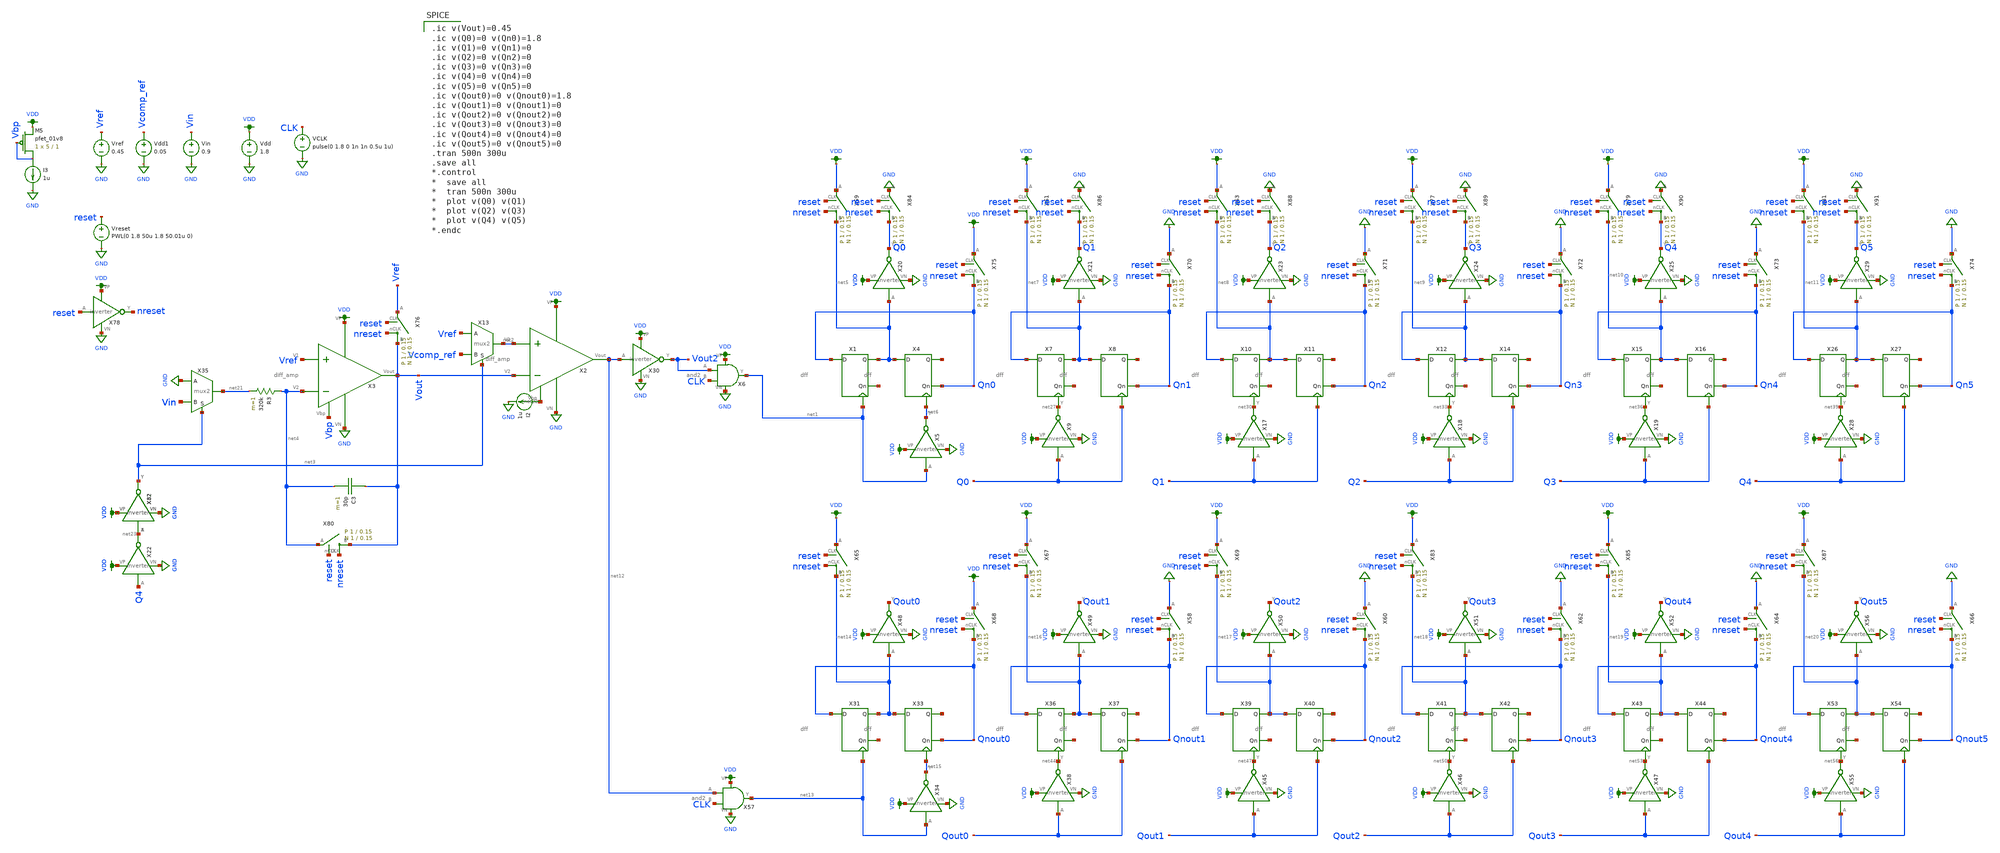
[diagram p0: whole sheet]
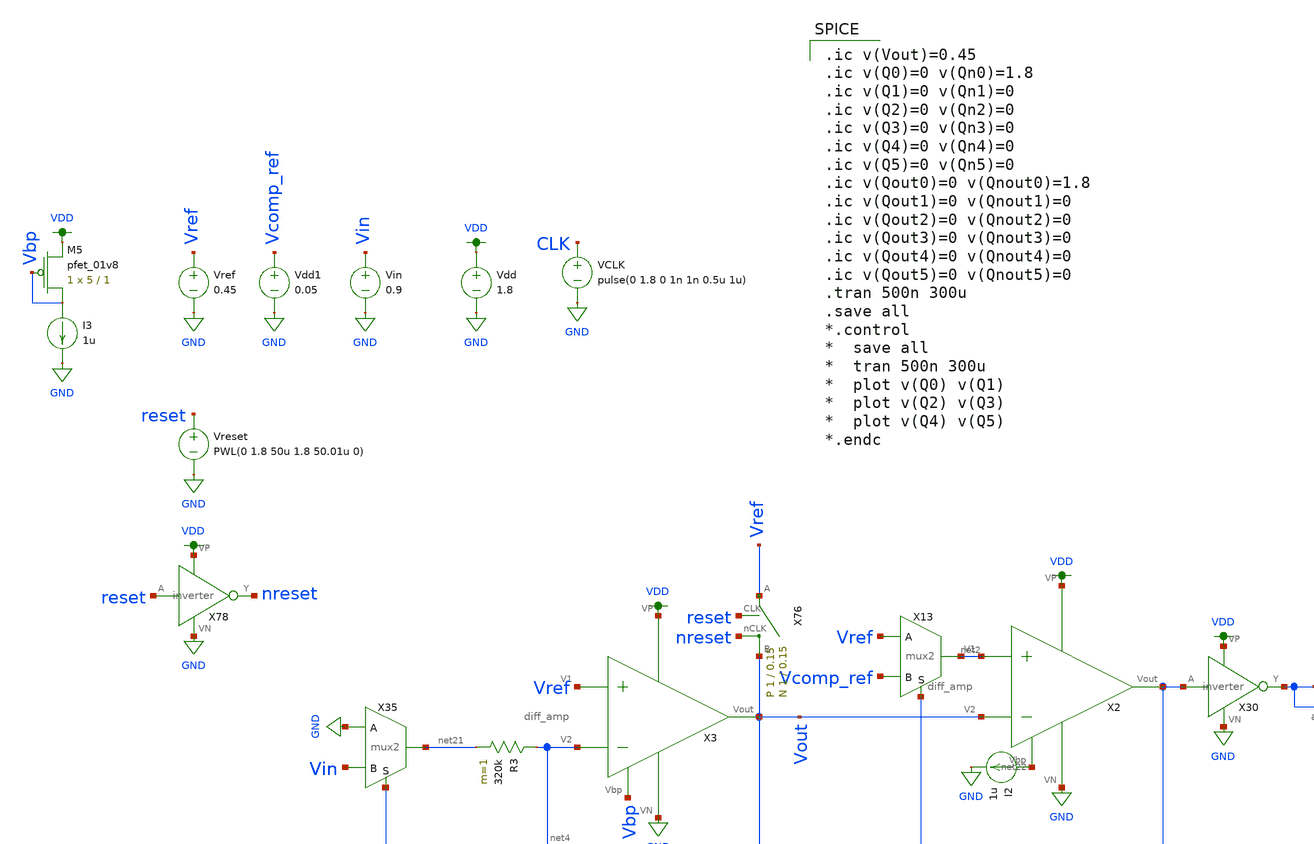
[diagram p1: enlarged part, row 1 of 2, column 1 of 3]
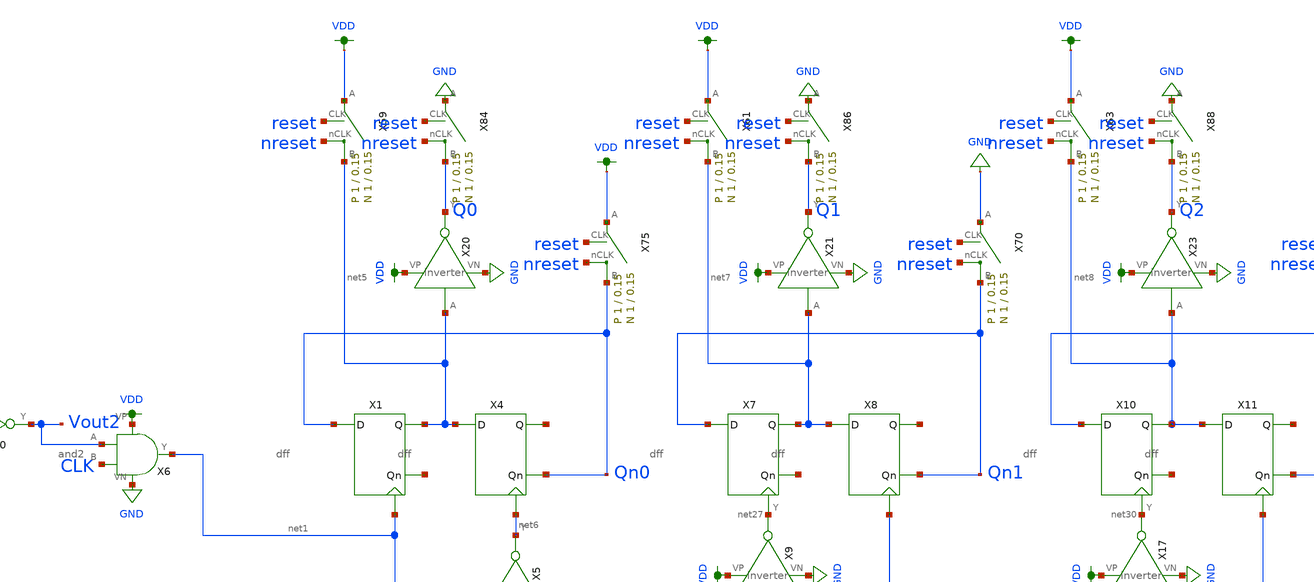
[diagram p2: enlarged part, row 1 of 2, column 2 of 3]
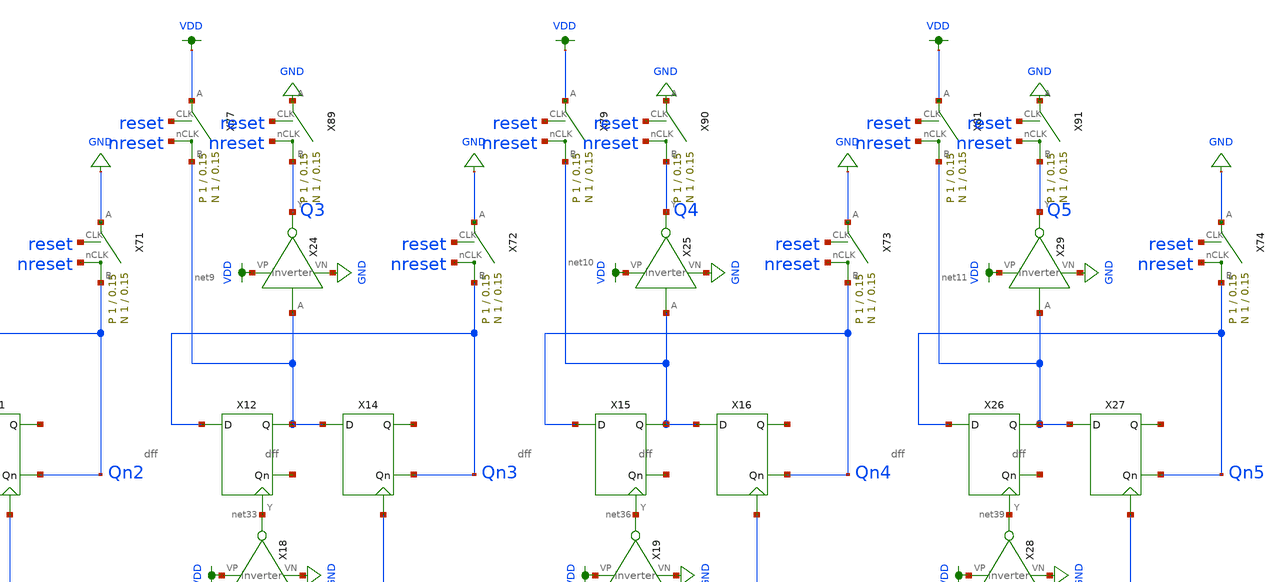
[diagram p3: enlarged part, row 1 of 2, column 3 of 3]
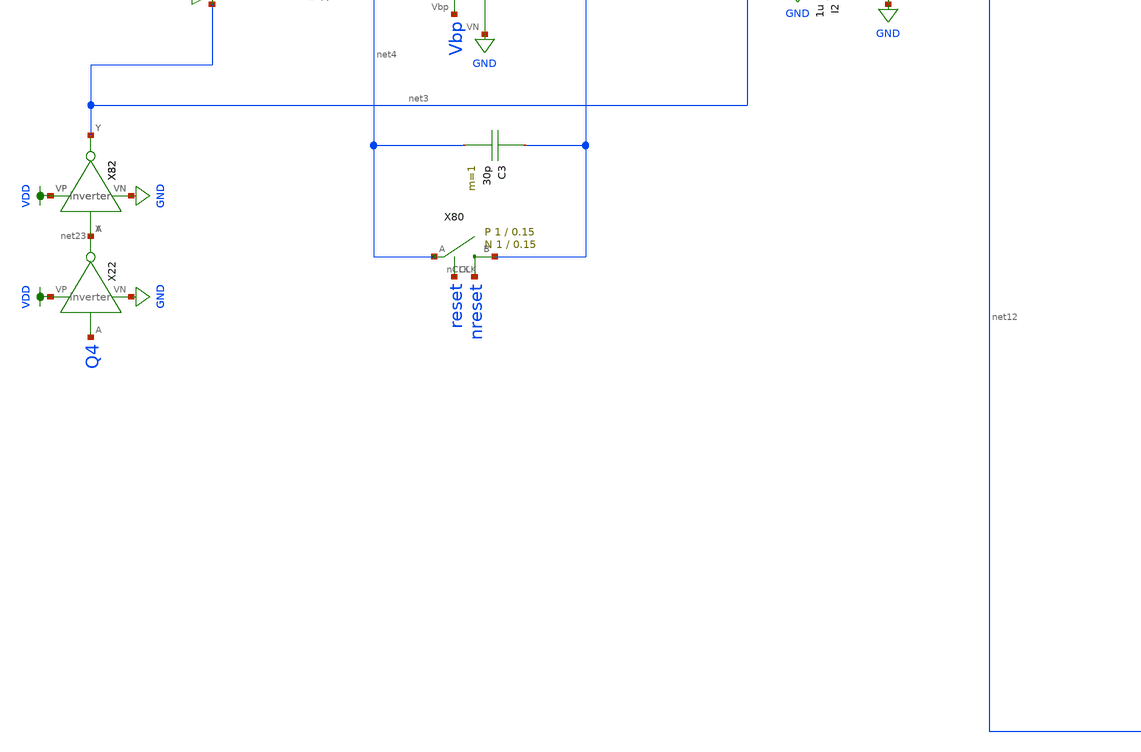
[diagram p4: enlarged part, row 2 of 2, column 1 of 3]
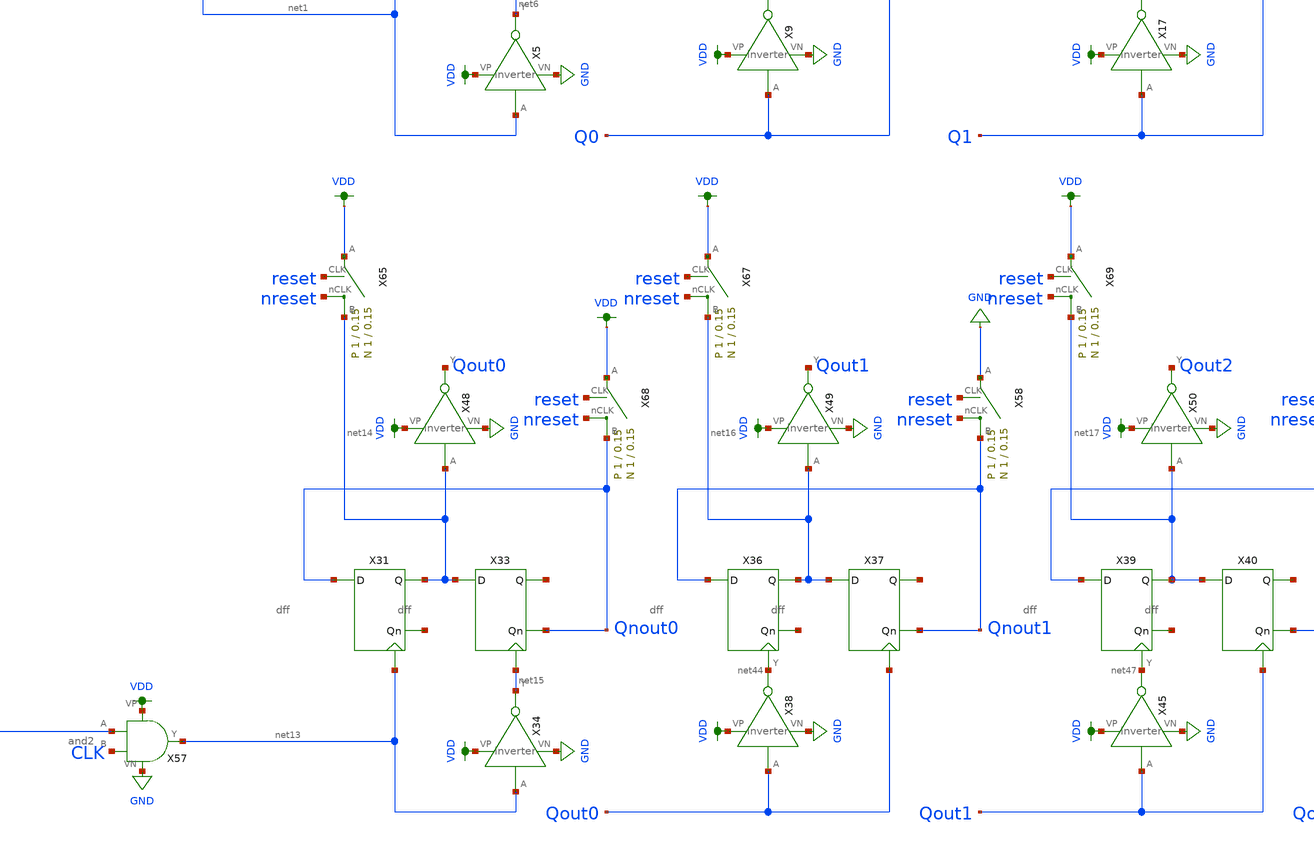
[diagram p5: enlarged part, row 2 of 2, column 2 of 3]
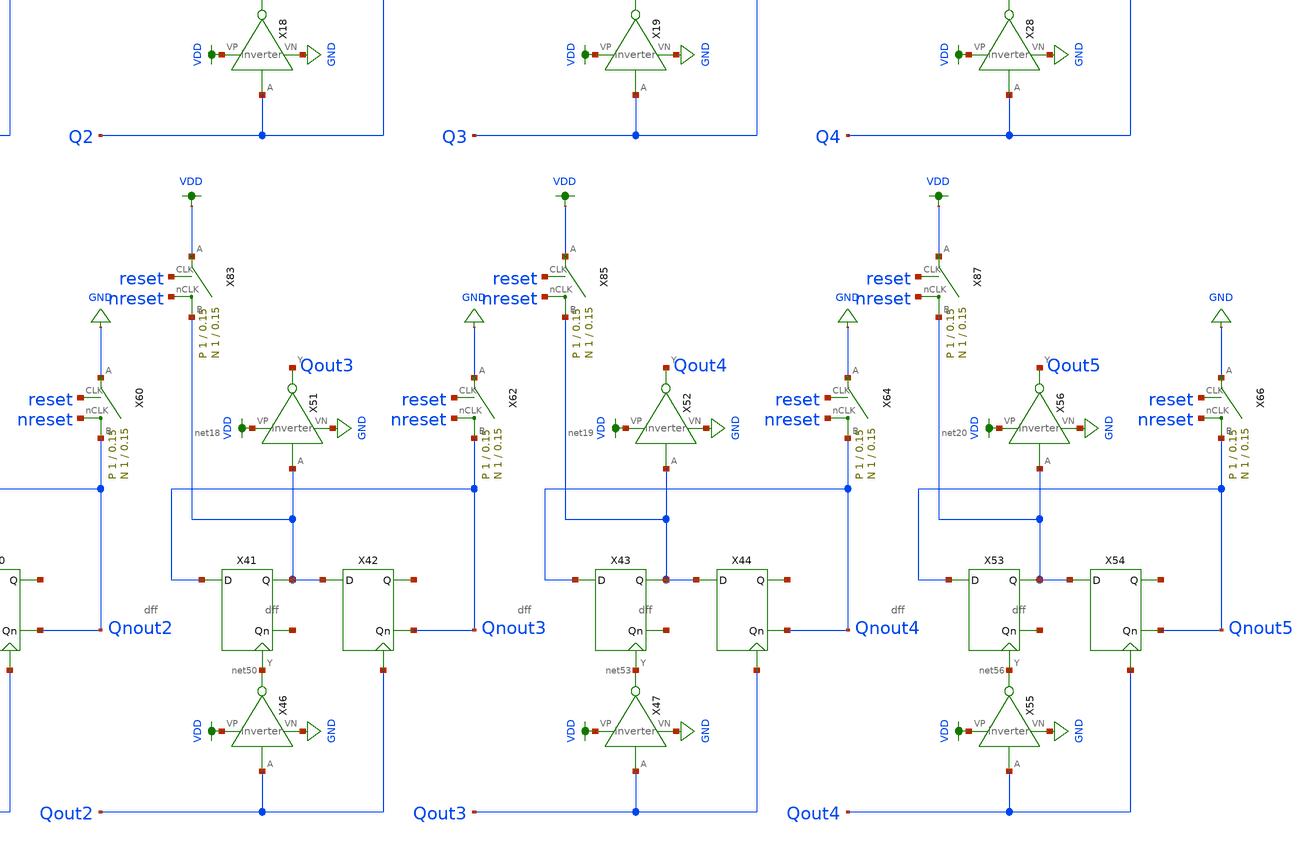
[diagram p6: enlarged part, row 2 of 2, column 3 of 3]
** sch_path: schematic/double-slope-works.sch
**.subckt double-slope-works
X2 VDD net22 net12 net2 Vout GND diff_amp
Vdd VDD GND 1.8
VCLK CLK GND pulse(0 1.8 0 1n 1n 0.5u 1u)
Vdd1 Vcomp_ref GND 0.05
Vin Vin GND 0.9
I2 net22 GND 1u
X6 VDD Vout2 GND net1 CLK and2
X13 net2 Vref Vcomp_ref net3 mux2
X22 Q4 net23 VDD GND inverter
X32 net23 net3 VDD GND inverter
X35 net21 GND Vin net3 mux2
XM5 Vbp Vbp VDD VDD sky130_fd_pr__pfet_01v8 L=1 W=5 nf=1 ad='int((nf+1)/2) * W/nf * 0.29' as='int((nf+2)/2) * W/nf * 0.29'
+ pd='2*int((nf+1)/2) * (W/nf + 0.29)' ps='2*int((nf+2)/2) * (W/nf + 0.29)' nrd='0.29 / W' nrs='0.29 / W'
+ sa=0 sb=0 sd=0 mult=1 m=1
I3 Vbp GND 1u
C3 Vout net4 30p m=1
X3 VDD Vbp Vout Vref net4 GND diff_amp
R3 net4 net21 320k m=1
Vref Vref GND 0.45
X1 Qn0 net24 net5 net1 dff
X4 net5 Qn0 net25 net6 dff
X5 net1 net6 VDD GND inverter
X7 Qn1 net26 net7 net27 dff
X8 net7 Qn1 net28 Q0 dff
X9 Q0 net27 VDD GND inverter
X10 Qn2 net29 net8 net30 dff
X11 net8 Qn2 net31 Q1 dff
X12 Qn3 net32 net9 net33 dff
X14 net9 Qn3 net34 Q2 dff
X15 Qn4 net35 net10 net36 dff
X16 net10 Qn4 net37 Q3 dff
X17 Q1 net30 VDD GND inverter
X18 Q2 net33 VDD GND inverter
X19 Q3 net36 VDD GND inverter
X20 net5 Q0 VDD GND inverter
X21 net7 Q1 VDD GND inverter
X23 net8 Q2 VDD GND inverter
X24 net9 Q3 VDD GND inverter
X25 net10 Q4 VDD GND inverter
X26 Qn5 net38 net11 net39 dff
X27 net11 Qn5 net40 Q4 dff
X28 Q4 net39 VDD GND inverter
X29 net11 Q5 VDD GND inverter
X30 net12 Vout2 VDD GND inverter
X31 Qnout0 net41 net14 net13 dff
X33 net14 Qnout0 net42 net15 dff
X34 net13 net15 VDD GND inverter
X36 Qnout1 net43 net16 net44 dff
X37 net16 Qnout1 net45 Qout0 dff
X38 Qout0 net44 VDD GND inverter
X39 Qnout2 net46 net17 net47 dff
X40 net17 Qnout2 net48 Qout1 dff
X41 Qnout3 net49 net18 net50 dff
X42 net18 Qnout3 net51 Qout2 dff
X43 Qnout4 net52 net19 net53 dff
X44 net19 Qnout4 net54 Qout3 dff
X45 Qout1 net47 VDD GND inverter
X46 Qout2 net50 VDD GND inverter
X47 Qout3 net53 VDD GND inverter
X48 net14 Qout0 VDD GND inverter
X49 net16 Qout1 VDD GND inverter
X50 net17 Qout2 VDD GND inverter
X51 net18 Qout3 VDD GND inverter
X52 net19 Qout4 VDD GND inverter
X53 Qnout5 net55 net20 net56 dff
X54 net20 Qnout5 net57 Qout4 dff
X55 Qout4 net56 VDD GND inverter
X56 net20 Qout5 VDD GND inverter
X57 VDD net12 GND net13 CLK and2
X70 Qn1 GND reset nreset switch Wp=1 Lp=0.15 WW=1 LL=0.15
X71 Qn2 GND reset nreset switch Wp=1 Lp=0.15 WW=1 LL=0.15
X72 Qn3 GND reset nreset switch Wp=1 Lp=0.15 WW=1 LL=0.15
X73 Qn4 GND reset nreset switch Wp=1 Lp=0.15 WW=1 LL=0.15
X74 Qn5 GND reset nreset switch Wp=1 Lp=0.15 WW=1 LL=0.15
X75 Qn0 VDD reset nreset switch Wp=1 Lp=0.15 WW=1 LL=0.15
X59 net5 VDD reset nreset switch Wp=1 Lp=0.15 WW=1 LL=0.15
X61 net7 VDD reset nreset switch Wp=1 Lp=0.15 WW=1 LL=0.15
X63 net8 VDD reset nreset switch Wp=1 Lp=0.15 WW=1 LL=0.15
X77 net9 VDD reset nreset switch Wp=1 Lp=0.15 WW=1 LL=0.15
X79 net10 VDD reset nreset switch Wp=1 Lp=0.15 WW=1 LL=0.15
X81 net11 VDD reset nreset switch Wp=1 Lp=0.15 WW=1 LL=0.15
X65 net14 VDD reset nreset switch Wp=1 Lp=0.15 WW=1 LL=0.15
X67 net16 VDD reset nreset switch Wp=1 Lp=0.15 WW=1 LL=0.15
X69 net17 VDD reset nreset switch Wp=1 Lp=0.15 WW=1 LL=0.15
X83 net18 VDD reset nreset switch Wp=1 Lp=0.15 WW=1 LL=0.15
X85 net19 VDD reset nreset switch Wp=1 Lp=0.15 WW=1 LL=0.15
X87 net20 VDD reset nreset switch Wp=1 Lp=0.15 WW=1 LL=0.15
X58 Qnout1 GND reset nreset switch Wp=1 Lp=0.15 WW=1 LL=0.15
X60 Qnout2 GND reset nreset switch Wp=1 Lp=0.15 WW=1 LL=0.15
X62 Qnout3 GND reset nreset switch Wp=1 Lp=0.15 WW=1 LL=0.15
X64 Qnout4 GND reset nreset switch Wp=1 Lp=0.15 WW=1 LL=0.15
X66 Qnout5 GND reset nreset switch Wp=1 Lp=0.15 WW=1 LL=0.15
X68 Qnout0 VDD reset nreset switch Wp=1 Lp=0.15 WW=1 LL=0.15
X76 Vout Vref reset nreset switch Wp=1 Lp=0.15 WW=1 LL=0.15
Vreset reset GND PWL(0 1.8 50u 1.8 50.01u 0)
X78 reset nreset VDD GND inverter
X80 Vout net4 reset nreset switch Wp=1 Lp=0.15 WW=1 LL=0.15
X82 net23 net3 VDD GND inverter
X84 Q0 GND reset nreset switch Wp=1 Lp=0.15 WW=1 LL=0.15
X86 Q1 GND reset nreset switch Wp=1 Lp=0.15 WW=1 LL=0.15
X88 Q2 GND reset nreset switch Wp=1 Lp=0.15 WW=1 LL=0.15
X89 Q3 GND reset nreset switch Wp=1 Lp=0.15 WW=1 LL=0.15
X90 Q4 GND reset nreset switch Wp=1 Lp=0.15 WW=1 LL=0.15
X91 Q5 GND reset nreset switch Wp=1 Lp=0.15 WW=1 LL=0.15
**** begin user architecture code

.ic v(Vout)=0.45
.ic v(Q0)=0 v(Qn0)=1.8
.ic v(Q1)=0 v(Qn1)=0
.ic v(Q2)=0 v(Qn2)=0
.ic v(Q3)=0 v(Qn3)=0
.ic v(Q4)=0 v(Qn4)=0
.ic v(Q5)=0 v(Qn5)=0
.ic v(Qout0)=0 v(Qnout0)=1.8
.ic v(Qout1)=0 v(Qnout1)=0
.ic v(Qout2)=0 v(Qnout2)=0
.ic v(Qout3)=0 v(Qnout3)=0
.ic v(Qout4)=0 v(Qnout4)=0
.ic v(Qout5)=0 v(Qnout5)=0
.tran 500n 300u
.save all
*.control
*  save all
*  tran 500n 300u
*  plot v(Q0) v(Q1)
*  plot v(Q2) v(Q3)
*  plot v(Q4) v(Q5)
*.endc


.option wnflag=1
.param MC_SWITCH=0.0
.lib ~/skywater/skywater-pdk/libraries/sky130_fd_pr_ngspice/latest/models/sky130.lib.spice tt

**** end user architecture code
**.ends
.GLOBAL GND
.GLOBAL VDD
.end
